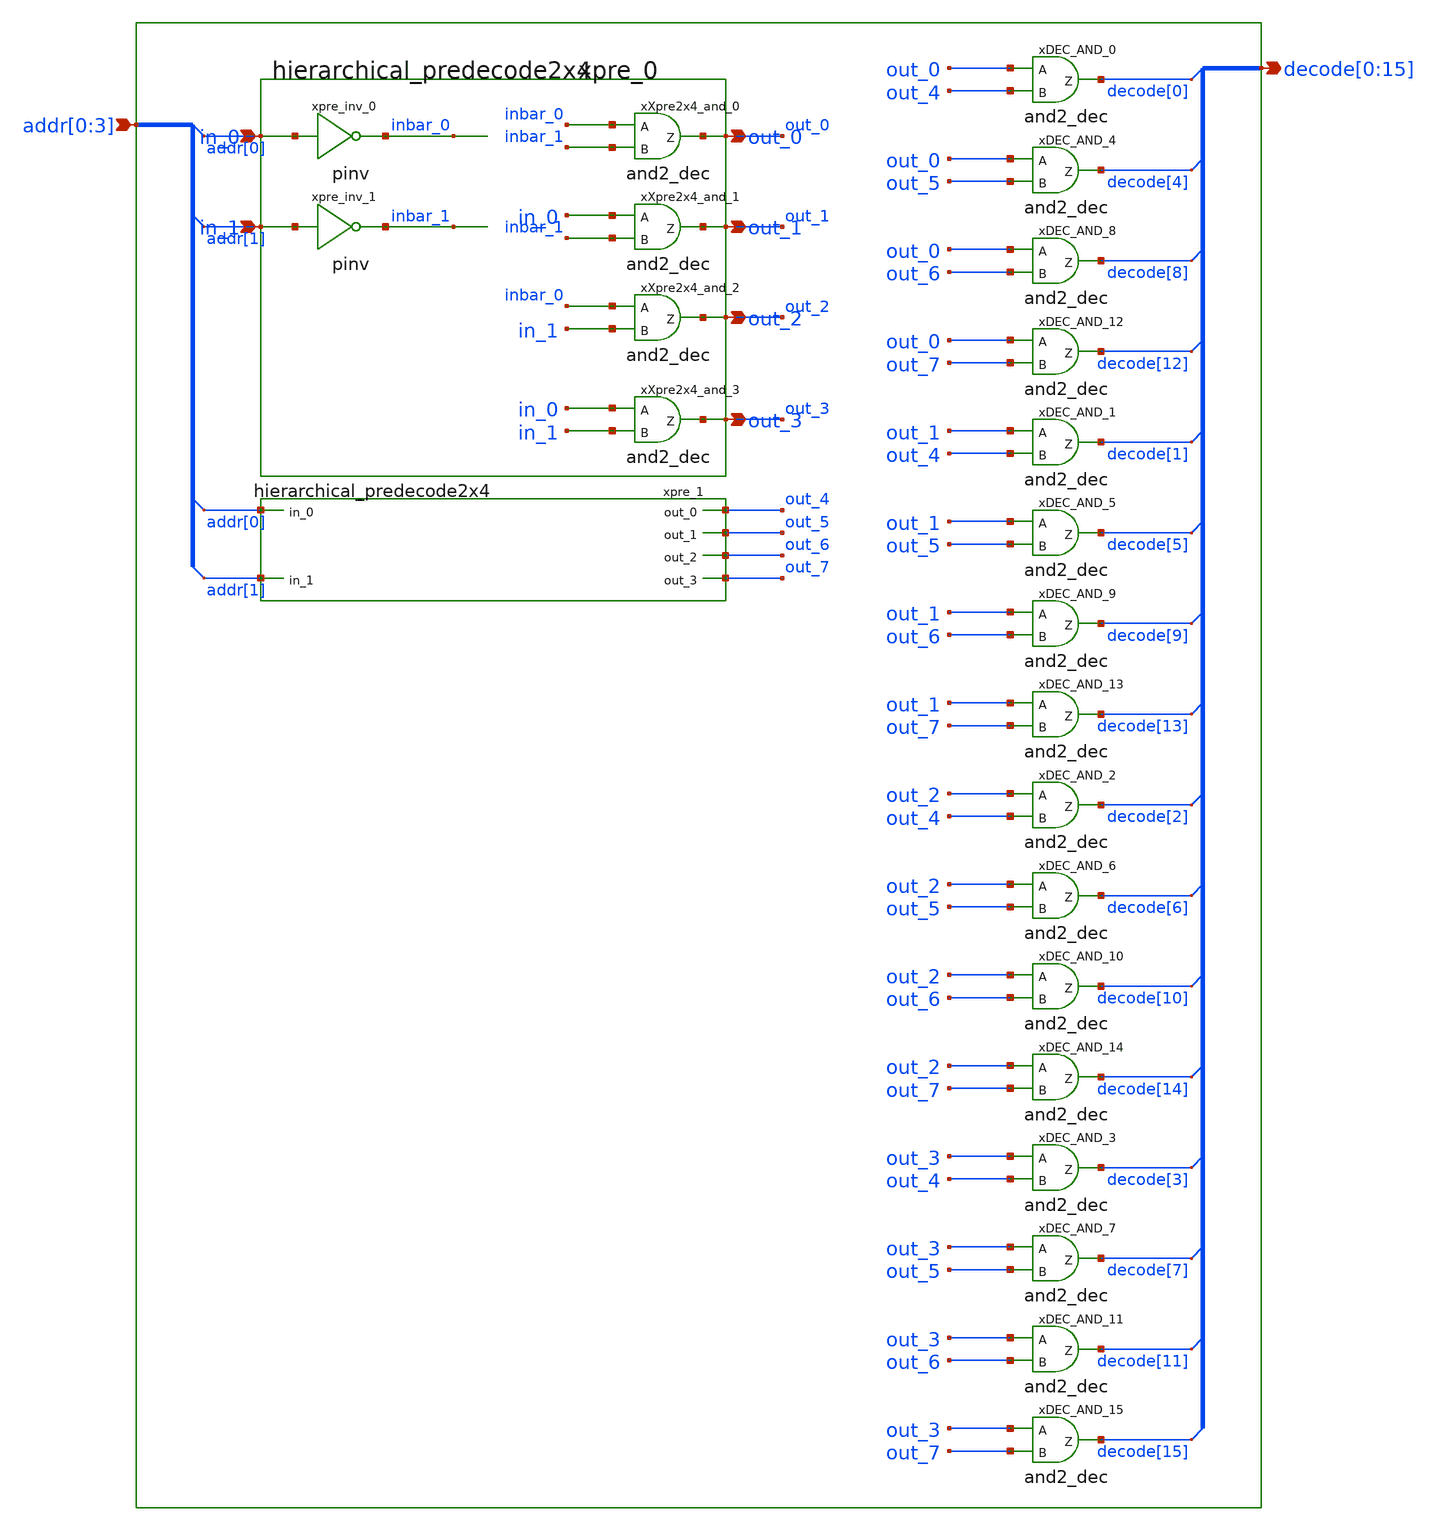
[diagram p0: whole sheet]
** sch_path: sram_4_16_scn4m/hierarchical_decoder.sch
**.subckt hierarchical_decoder addr[0],addr[1],addr[2],addr[3]
*+ decode[0],decode[1],decode[2],decode[3],decode[4],decode[5],decode[6],decode[7],decode[8],decode[9],decode[10],decode[11],decode[12],decode[13],decode[14],decode[15]
*.ipin addr[0],addr[1],addr[2],addr[3]
*.opin
*+ decode[0],decode[1],decode[2],decode[3],decode[4],decode[5],decode[6],decode[7],decode[8],decode[9],decode[10],decode[11],decode[12],decode[13],decode[14],decode[15]
xpre_0 addr[0] addr[1] out_0 out_1 out_2 out_3 vdd gnd hierarchical_predecode2x4
xpre_1 addr[0] addr[1] out_4 out_5 out_6 out_7 vdd gnd hierarchical_predecode2x4
xDEC_AND_0 out_0 out_4 decode[0] and2_dec
xDEC_AND_4 out_0 out_5 decode[4] and2_dec
xDEC_AND_8 out_0 out_6 decode[8] and2_dec
xDEC_AND_12 out_0 out_7 decode[12] and2_dec
xDEC_AND_1 out_1 out_4 decode[1] and2_dec
xDEC_AND_5 out_1 out_5 decode[5] and2_dec
xDEC_AND_9 out_1 out_6 decode[9] and2_dec
xDEC_AND_13 out_1 out_7 decode[13] and2_dec
xDEC_AND_2 out_2 out_4 decode[2] and2_dec
xDEC_AND_6 out_2 out_5 decode[6] and2_dec
xDEC_AND_10 out_2 out_6 decode[10] and2_dec
xDEC_AND_14 out_2 out_7 decode[14] and2_dec
xDEC_AND_3 out_3 out_4 decode[3] and2_dec
xDEC_AND_7 out_3 out_5 decode[7] and2_dec
xDEC_AND_11 out_3 out_6 decode[11] and2_dec
xDEC_AND_15 out_3 out_7 decode[15] and2_dec
**.ends

* expanding   symbol:  hierarchical_predecode2x4.sch # of pins=6
** sym_path: sram_4_16_scn4m/hierarchical_predecode2x4.sch
** sch_path: sram_4_16_scn4m/hierarchical_predecode2x4.sch
.subckt hierarchical_predecode2x4 in_0 in_1 out_0 out_1 out_2 out_3 vdd gnd
*.ipin in_0
*.ipin in_1
*.opin out_0
*.opin out_1
*.opin out_2
*.opin out_3
xpre_inv_0 in_0 inbar_0 vdd gnd pinv
xpre_inv_1 in_1 inbar_1 vdd gnd pinv
xXpre2x4_and_0 inbar_0 inbar_1 out_0 and2_dec
xXpre2x4_and_1 in_0 inbar_1 out_1 and2_dec
xXpre2x4_and_2 inbar_0 in_1 out_2 and2_dec
xXpre2x4_and_3 in_0 in_1 out_3 and2_dec
.ends


* expanding   symbol:  and2_dec.sym # of pins=3
** sym_path: sram_4_16_scn4m/and2_dec.sym
** sch_path: sram_4_16_scn4m/and2_dec.sch
.subckt and2_dec A B Z
*.ipin A
*.ipin B
*.opin Z
xpand2_dec_nand A B zb_int vdd gnd pnand2
xpand2_dec_inv zb_int Z vdd gnd pinv
.ends


* expanding   symbol:  pinv.sym # of pins=2
** sym_path: sram_4_16_scn4m/pinv.sym
** sch_path: sram_4_16_scn4m/pinv.sch
.subckt pinv A Z vdd gnd
*.ipin A
*.opin Z
XMpinv_nmos Z A gnd gnd sky130_fd_pr__nfet_01v8 L=0.4 W=0.8 nf=1 ad='int((nf+1)/2) * W/nf * 0.29' as='int((nf+2)/2) * W/nf * 0.29'
+ pd='2*int((nf+1)/2) * (W/nf + 0.29)' ps='2*int((nf+2)/2) * (W/nf + 0.29)' nrd='0.29 / W' nrs='0.29 / W'
+ sa=0 sb=0 sd=0 mult=1 m=1
XMp_inv_pmos Z A vdd vdd sky130_fd_pr__pfet_01v8 L=0.4 W=1.6 nf=1 ad='int((nf+1)/2) * W/nf * 0.29' as='int((nf+2)/2) * W/nf * 0.29'
+ pd='2*int((nf+1)/2) * (W/nf + 0.29)' ps='2*int((nf+2)/2) * (W/nf + 0.29)' nrd='0.29 / W' nrs='0.29 / W'
+ sa=0 sb=0 sd=0 mult=1 m=1
.ends


* expanding   symbol:  pnand2.sym # of pins=3
** sym_path: sram_2_64_scn4m/pnand2.sym
** sch_path: sram_2_64_scn4m/pnand2.sch
.subckt pnand2 A B Z vdd gnd
*.ipin A
*.ipin B
*.opin Z
*.iopin vdd
*.iopin gnd
XMpnand2_nmos1 Z B net1 gnd sky130_fd_pr__nfet_01v8 L=0.4 W=1.6 nf=1 ad='int((nf+1)/2) * W/nf * 0.29'
+ as='int((nf+2)/2) * W/nf * 0.29' pd='2*int((nf+1)/2) * (W/nf + 0.29)' ps='2*int((nf+2)/2) * (W/nf + 0.29)'
+ nrd='0.29 / W' nrs='0.29 / W' sa=0 sb=0 sd=0 mult=1 m=1
XMpnand2_pmos1 Z A vdd vdd sky130_fd_pr__pfet_01v8 L=0.4 W=1.6 nf=1 ad='int((nf+1)/2) * W/nf * 0.29'
+ as='int((nf+2)/2) * W/nf * 0.29' pd='2*int((nf+1)/2) * (W/nf + 0.29)' ps='2*int((nf+2)/2) * (W/nf + 0.29)'
+ nrd='0.29 / W' nrs='0.29 / W' sa=0 sb=0 sd=0 mult=1 m=1
XMpnand2_pmos2 Z B vdd vdd sky130_fd_pr__pfet_01v8 L=0.4 W=1.6 nf=1 ad='int((nf+1)/2) * W/nf * 0.29'
+ as='int((nf+2)/2) * W/nf * 0.29' pd='2*int((nf+1)/2) * (W/nf + 0.29)' ps='2*int((nf+2)/2) * (W/nf + 0.29)'
+ nrd='0.29 / W' nrs='0.29 / W' sa=0 sb=0 sd=0 mult=1 m=1
XMpnand2_nmos2 net1 A gnd gnd sky130_fd_pr__nfet_01v8 L=0.4 W=1.6 nf=1 ad='int((nf+1)/2) * W/nf * 0.29'
+ as='int((nf+2)/2) * W/nf * 0.29' pd='2*int((nf+1)/2) * (W/nf + 0.29)' ps='2*int((nf+2)/2) * (W/nf + 0.29)'
+ nrd='0.29 / W' nrs='0.29 / W' sa=0 sb=0 sd=0 mult=1 m=1
.ends

.end
